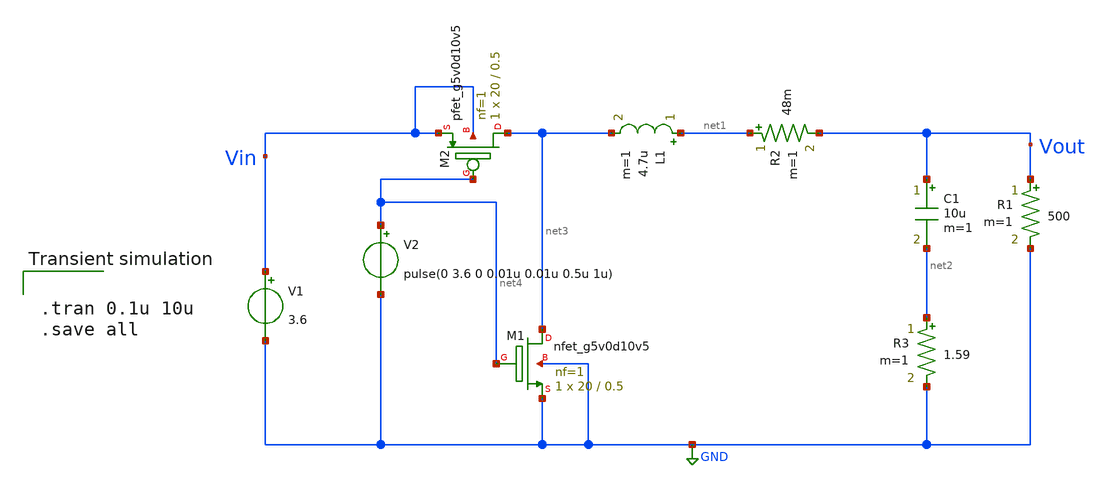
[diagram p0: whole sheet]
** sch_path: Abishek_Sam_group/Buck_converter.sch
**.subckt Buck_converter
XM1 net3 net4 GND GND sky130_fd_pr__nfet_g5v0d10v5 L=0.5 W=20 nf=1 ad='int((nf+1)/2) * W/nf * 0.29' as='int((nf+2)/2) * W/nf * 0.29'
+ pd='2*int((nf+1)/2) * (W/nf + 0.29)' ps='2*int((nf+2)/2) * (W/nf + 0.29)' nrd='0.29 / W' nrs='0.29 / W'
+ sa=0 sb=0 sd=0 mult=1 m=1
XM2 net3 net4 Vin Vin sky130_fd_pr__pfet_g5v0d10v5 L=0.5 W=20 nf=1 ad='int((nf+1)/2) * W/nf * 0.29' as='int((nf+2)/2) * W/nf * 0.29'
+ pd='2*int((nf+1)/2) * (W/nf + 0.29)' ps='2*int((nf+2)/2) * (W/nf + 0.29)' nrd='0.29 / W' nrs='0.29 / W'
+ sa=0 sb=0 sd=0 mult=1 m=1
C1 Vout net2 10u m=1
L1 net1 net3 4.7u m=1
R1 Vout GND 500 m=1
V1 Vin GND 3.6
R2 net1 Vout 48m m=1
R3 net2 GND 1.59 m=1
V2 net4 GND pulse(0 3.6 0 0.01u 0.01u 0.5u 1u)
**** begin user architecture code

.lib $::SKYWATER_MODELS/sky130.lib.spice tt

**** end user architecture code
**.ends
.GLOBAL GND
**** begin user architecture code


.tran 0.1u 10u
.save all


**** end user architecture code
.end
